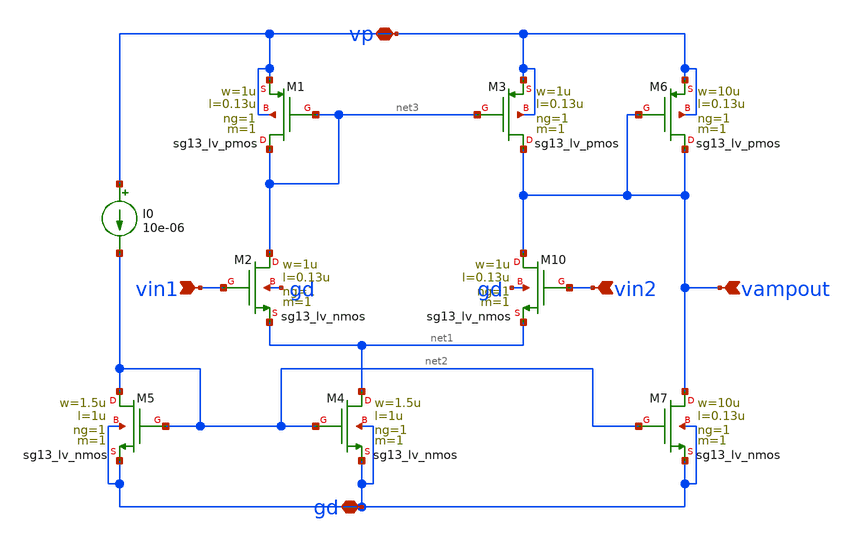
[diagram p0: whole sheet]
** sch_path: PLL0663-main/schematic/xschem/charge_pump/old_sch/amp.sch
**.subckt amp vin1 vin2 vampout vp gd
*.ipin vin1
*.ipin vin2
*.ipin vampout
*.iopin vp
*.iopin gd
XM3 vampout net3 vp vp sg13_lv_pmos w=1u l=0.13u ng=1 m=1 mm_ok=1
XM10 vampout vin2 net1 gd sg13_lv_nmos w=1u l=0.13u ng=1 m=1 mm_ok=1
XM1 net3 net3 vp vp sg13_lv_pmos w=1u l=0.13u ng=1 m=1 mm_ok=1
XM2 net3 vin1 net1 gd sg13_lv_nmos w=1u l=0.13u ng=1 m=1 mm_ok=1
XM4 net1 net2 gd gd sg13_lv_nmos w=1.5u l=1u ng=1 m=1 mm_ok=1
XM5 net2 net2 gd gd sg13_lv_nmos w=1.5u l=1u ng=1 m=1 mm_ok=1
XM6 vampout vampout vp vp sg13_lv_pmos w=10u l=0.13u ng=1 m=1 mm_ok=1
XM7 vampout net2 gd gd sg13_lv_nmos w=10u l=0.13u ng=1 m=1 mm_ok=1
I0 vp net2 10e-06
**.ends
.end
